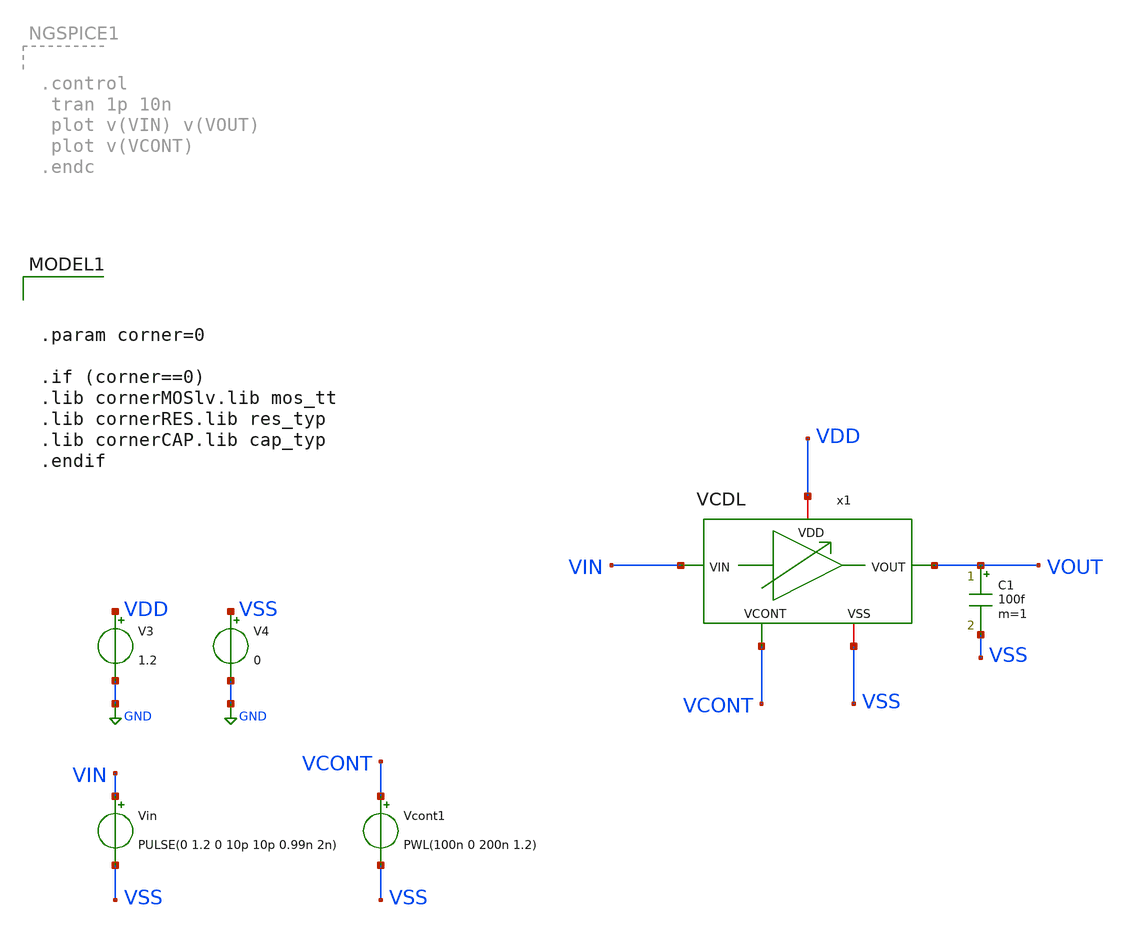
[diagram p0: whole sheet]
** sch_path: testbenchs/tb_VCDL.sch
**.subckt tb_VCDL
Vin VIN VSS PULSE(0 1.2 0 10p 10p 0.99n 2n)
C1 VOUT VSS 100f m=1
Vcont1 VCONT VSS PWL(100n 0 200n 1.2)
x1 VDD VIN VOUT VCONT VSS VCDL
V3 VDD GND 1.2
V4 VSS GND 0
**** begin user architecture code


.param corner=0

.if (corner==0)
.lib cornerMOSlv.lib mos_tt
.lib cornerRES.lib res_typ
.lib cornerCAP.lib cap_typ
.endif



.control
* ---- settings you tweak ----


   * ---- user settings ----
  let vlow  = 0
  let vhigh = 1.2
  let v50   = vlow + 0.5*(vhigh - vlow)

  let start_edge = 0     ; skip early edges (settling)
  let N = 200             ; number of phase samples



  tran 2p 200n

 * ---- allocate vectors ----
  let tvec   = vector(N)
  let phivec = vector(N)
  let vcontvec  = vector(N)

  let k = 0
  let i = start_edge

  while k < N
    * crossing times
    meas tran tin      WHEN v(VIN)=v50  RISE=i
    meas tran tout     WHEN v(VOUT)=v50 RISE=i
    meas tran tin_next WHEN v(VIN)=v50  RISE=(i+1)

    * delay + period
    let dt = tout - tin
    let T  = tin_next - tin

    * phase in degrees (per-cycle)
    let phi = 360*dt/T
    let phi = phi - 360*floor(phi/360)

    *let vc = value(v(VCONT), tin)
    meas tran vc FIND v(VCONT) AT=tin
    let vcontvec[k] = vc
    * store sample at time = tin
    let tvec[k]   = tin
    let phivec[k] = phi
    let vcontvec[k] = vc

    let k = k + 1
    let i = i + 1
  end

  * plot phase vs time (one point per cycle)
  plot phivec vs tvec
  plot phivec vs vcontvec
.endc


**** end user architecture code
**.ends

* expanding   symbol:  /foss/designs/DLL/2026/Cells/VCDL.sym # of pins=5
** sym_path: /foss/designs/DLL/2026/Cells/VCDL.sym
** sch_path: /foss/designs/DLL/2026/Cells/VCDL.sch
.subckt VCDL VDD VIN VOUT VCONT VSS
*.iopin VDD
*.iopin VSS
*.ipin VIN
*.ipin VCONT
*.opin VOUT
XM1 VOUT VIN net3 VSS sg13_lv_nmos w=2u l=0.13u ng=1 m=1 mm_ok=1
XM2 net3 VCONT VSS VSS sg13_lv_nmos w=3.5u l=0.16u ng=1 m=1 mm_ok=1
XM3 net1 VCONT VSS VSS sg13_lv_nmos w=2u l=0.25u ng=1 m=1 mm_ok=1
XM4 VOUT VIN net2 VDD sg13_lv_pmos w=4.5u l=0.13u ng=1 m=1 mm_ok=1
XM5 net2 net1 VDD VDD sg13_lv_pmos w=3u l=0.16u ng=1 m=1 mm_ok=1
XM6 net1 net1 VDD VDD sg13_lv_pmos w=2.24u l=0.13u ng=1 m=1 mm_ok=1
.ends

.GLOBAL GND
.end
